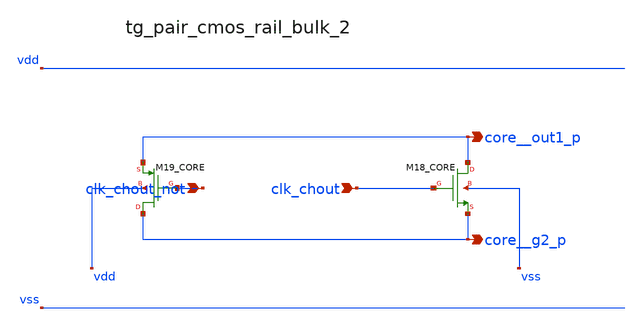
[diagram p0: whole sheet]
** sch_path: analog-db/raw/ia_006_fan_chopper_cmfb/hier/blocks/tg_pair_cmos_rail_bulk_2.sch
**.subckt tg_pair_cmos_rail_bulk_2 clk_chout_not clk_chout core__out1_p core__g2_p
*.ipin clk_chout_not
*.ipin clk_chout
*.opin core__out1_p
*.opin core__g2_p
XM18_CORE core__out1_p clk_chout core__g2_p vss sg13_lv_nmos w=x_dut_xm18_core_w l=x_dut_xm18_core_l
+ ng=1 m=x_dut_xm18_core_m
XM19_CORE core__g2_p clk_chout_not core__out1_p vdd sg13_lv_pmos w=x_dut_xm19_core_w
+ l=x_dut_xm19_core_l ng=1 m=x_dut_xm19_core_m
**.ends
.end
